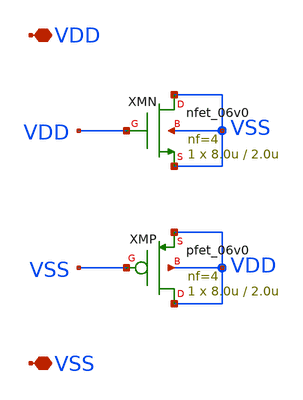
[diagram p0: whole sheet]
** sch_path: FINAL/XSCHEM/DECAP/DECAP.sch
**.subckt DECAP VDD VSS
*.iopin VDD
*.iopin VSS
XMN VSS VDD VSS VSS nfet_06v0 L=2.0u W=8.0u nf=4 ad='int((nf+1)/2) * W/nf * 0.18u' as='int((nf+2)/2) * W/nf * 0.18u'
+ pd='2*int((nf+1)/2) * (W/nf + 0.18u)' ps='2*int((nf+2)/2) * (W/nf + 0.18u)' nrd='0.18u / W' nrs='0.18u / W'
+ sa=0 sb=0 sd=0 m=1
XMP VDD VSS VDD VDD pfet_06v0 L=2.0u W=8.0u nf=4 ad='int((nf+1)/2) * W/nf * 0.18u' as='int((nf+2)/2) * W/nf * 0.18u'
+ pd='2*int((nf+1)/2) * (W/nf + 0.18u)' ps='2*int((nf+2)/2) * (W/nf + 0.18u)' nrd='0.18u / W' nrs='0.18u / W'
+ sa=0 sb=0 sd=0 m=1
**.ends
.end
